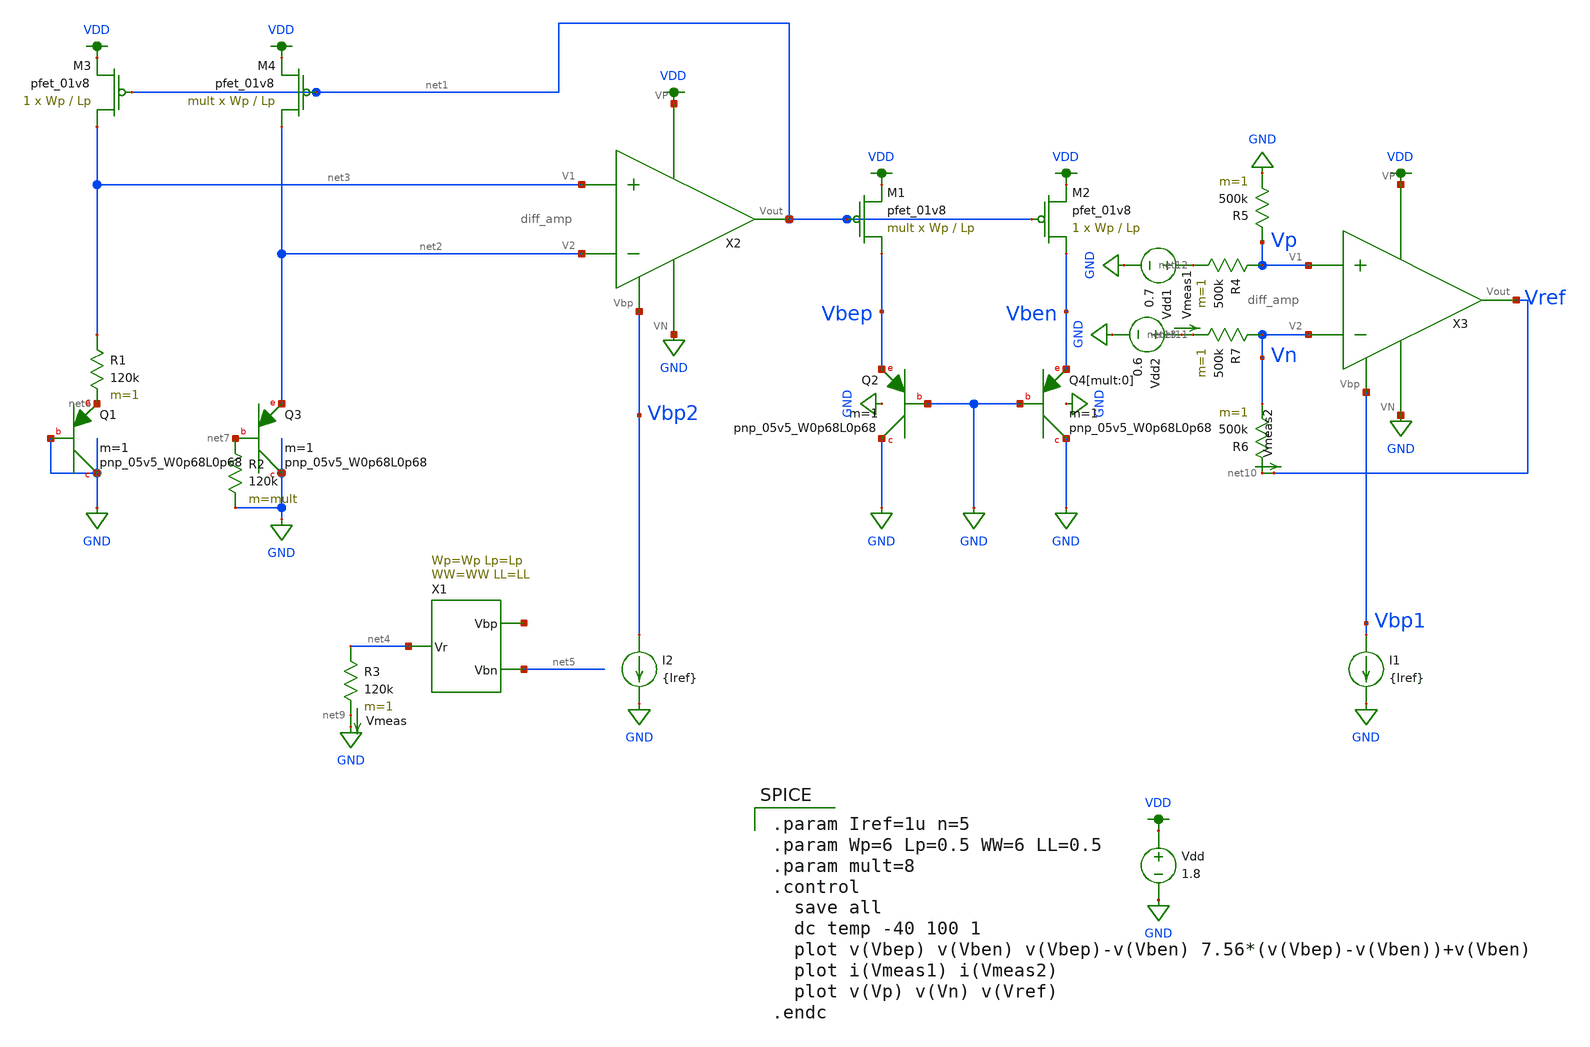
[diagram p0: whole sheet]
** sch_path: schematic/test/bandgap_dctemp.sch
**.subckt bandgap_dctemp
XQ2 GND GND Vbep sky130_fd_pr__pnp_05v5_W0p68L0p68 m=1
Vdd VDD GND 1.8
XM1 Vbep net1 VDD VDD sky130_fd_pr__pfet_01v8 L=Lp W=Wp nf=1 ad='int((nf+1)/2) * W/nf * 0.29' as='int((nf+2)/2) * W/nf * 0.29'
+ pd='2*int((nf+1)/2) * (W/nf + 0.29)' ps='2*int((nf+2)/2) * (W/nf + 0.29)' nrd='0.29 / W' nrs='0.29 / W'
+ sa=0 sb=0 sd=0 mult=mult m=mult
XM2 Vben net1 VDD VDD sky130_fd_pr__pfet_01v8 L=Lp W=Wp nf=1 ad='int((nf+1)/2) * W/nf * 0.29' as='int((nf+2)/2) * W/nf * 0.29'
+ pd='2*int((nf+1)/2) * (W/nf + 0.29)' ps='2*int((nf+2)/2) * (W/nf + 0.29)' nrd='0.29 / W' nrs='0.29 / W'
+ sa=0 sb=0 sd=0 mult=1 m=1
XQ4[mult:0] GND GND Vben sky130_fd_pr__pnp_05v5_W0p68L0p68 m=1
XQ1 GND GND net6 sky130_fd_pr__pnp_05v5_W0p68L0p68 m=1
XQ3 GND net7 net2 sky130_fd_pr__pnp_05v5_W0p68L0p68 m=1
R1 net3 net6 120k m=1
R2 net7 GND 120k m=mult
XM3 net3 net1 VDD VDD sky130_fd_pr__pfet_01v8 L=Lp W=Wp nf=1 ad='int((nf+1)/2) * W/nf * 0.29' as='int((nf+2)/2) * W/nf * 0.29'
+ pd='2*int((nf+1)/2) * (W/nf + 0.29)' ps='2*int((nf+2)/2) * (W/nf + 0.29)' nrd='0.29 / W' nrs='0.29 / W'
+ sa=0 sb=0 sd=0 mult=1 m=1
XM4 net2 net1 VDD VDD sky130_fd_pr__pfet_01v8 L=Lp W=Wp nf=1 ad='int((nf+1)/2) * W/nf * 0.29' as='int((nf+2)/2) * W/nf * 0.29'
+ pd='2*int((nf+1)/2) * (W/nf + 0.29)' ps='2*int((nf+2)/2) * (W/nf + 0.29)' nrd='0.29 / W' nrs='0.29 / W'
+ sa=0 sb=0 sd=0 mult=mult m=mult
X1 net4 net5 net8 ibias Wp=Wp Lp=Lp WW=WW LL=LL
R3 net4 net9 120k m=1
Vmeas net9 GND 0
.save i(vmeas)
R6 net10 Vn 500k m=1
X3 VDD Vbp1 Vref Vp Vn GND diff_amp
X2 VDD Vbp2 net1 net3 net2 GND diff_amp
R7 Vn net11 500k m=1
R4 Vp net12 500k m=1
R5 Vp GND 500k m=1
Vmeas1 net13 net11 0
.save i(vmeas1)
Vmeas2 net10 Vref 0
.save i(vmeas2)
Vdd1 net12 GND 0.7
Vdd2 net13 GND 0.6
I1 Vbp1 GND {Iref}
I2 Vbp2 GND {Iref}
**** begin user architecture code

.option wnflag=1
.param MC_SWITCH=0.0
.lib /media/qdeng/526448C32060CF5C/skywater/skywater-pdk/libraries/sky130_fd_pr_ngspice/latest/models/sky130.lib.spice tt


.param Iref=1u n=5
.param Wp=6 Lp=0.5 WW=6 LL=0.5
.param mult=8
.control
  save all
  dc temp -40 100 1
  plot v(Vbep) v(Vben) v(Vbep)-v(Vben) 7.56*(v(Vbep)-v(Vben))+v(Vben)
  plot i(Vmeas1) i(Vmeas2)
  plot v(Vp) v(Vn) v(Vref)
.endc

**** end user architecture code
**.ends
.GLOBAL GND
.GLOBAL VDD
.end
